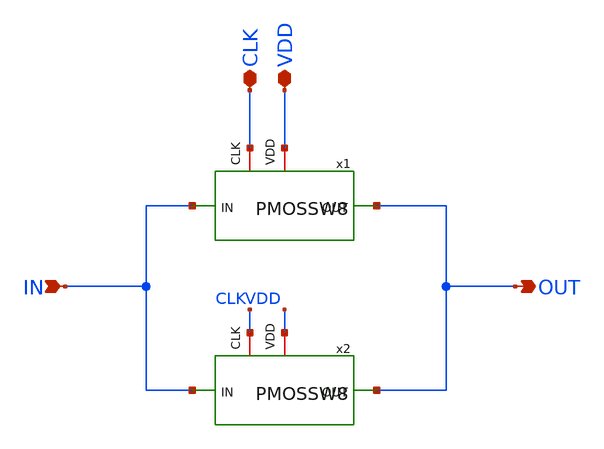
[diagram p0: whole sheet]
** sch_path: PMOSSW16.sch
**.subckt PMOSSW16 IN OUT CLK VDD
*.ipin IN
*.opin OUT
*.iopin CLK
*.iopin VDD
x1 CLK OUT IN VDD PMOSSW8
x2 CLK OUT IN VDD PMOSSW8
**.ends

* expanding   symbol:  PMOSSW8.sym # of pins=4
** sym_path: PMOSSW8.sym
** sch_path: PMOSSW8.sch
.subckt PMOSSW8 CLK OUT IN VDD
*.ipin IN
*.opin OUT
*.iopin CLK
*.iopin VDD
x1 CLK OUT IN VDD PMOSSW4
x2 CLK OUT IN VDD PMOSSW4
.ends


* expanding   symbol:  PMOSSW4.sym # of pins=4
** sym_path: PMOSSW4.sym
** sch_path: PMOSSW4.sch
.subckt PMOSSW4 CLK OUT IN VDD
*.ipin IN
*.opin OUT
*.iopin CLK
*.iopin VDD
x1 CLK OUT IN VDD PMOSSW2
x2 CLK OUT IN VDD PMOSSW2
.ends


* expanding   symbol:  PMOSSW2.sym # of pins=4
** sym_path: PMOSSW2.sym
** sch_path: PMOSSW2.sch
.subckt PMOSSW2 CLK OUT IN VDD
*.ipin IN
*.opin OUT
*.iopin CLK
*.iopin VDD
x1 CLK OUT IN VDD PMOSSW
x2 CLK OUT IN VDD PMOSSW
.ends


* expanding   symbol:  PMOSSW.sym # of pins=4
** sym_path: PMOSSW.sym
** sch_path: PMOSSW.sch
.subckt PMOSSW CLK OUT IN VDD
*.ipin IN
*.opin OUT
*.iopin VDD
*.iopin CLK
M5 OUT CLK IN VDD pch w=10u l=0.35u as=0 ps=0 ad=0 pd=0 m=1
.ends

.end
